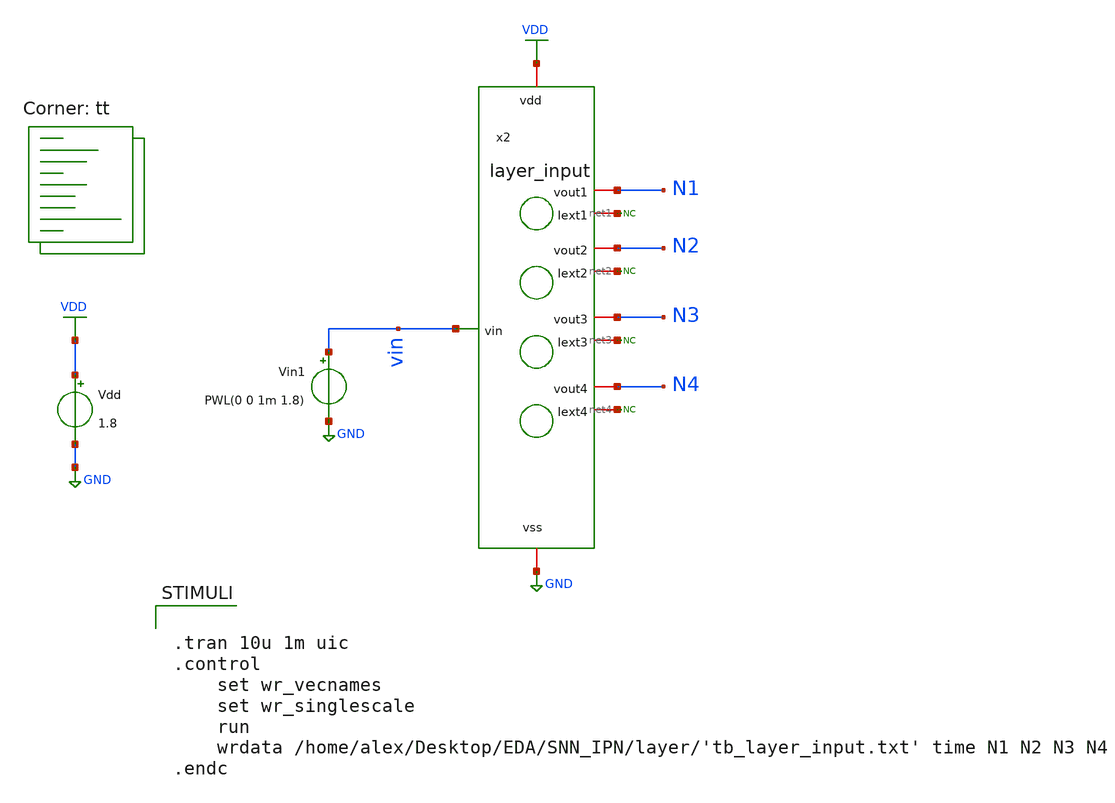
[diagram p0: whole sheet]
** sch_path: layer/tb_layer_input.sch
**.subckt tb_layer_input
x2 VDD GND vin N1 N2 N3 N4 net1 net2 net3 net4 layer_input
Vin1 vin GND PWL(0 0 1m 1.8)
* noconn #net1
* noconn #net2
* noconn #net3
* noconn #net4
Vdd VDD GND 1.8
**** begin user architecture code
.lib $::SKYWATER_MODELS/sky130.lib.spice tt
**** end user architecture code
**.ends

* expanding   symbol:  layer/layer_input.sym # of pins=11
** sym_path: layer/layer_input.sym
** sch_path: layer/layer_input.sch
.subckt layer_input vdd vss vin vout1 vout2 vout3 vout4 Iext1 Iext2 Iext3 Iext4
*.iopin vdd
*.iopin vss
*.ipin vin
*.iopin vout1
*.iopin vout2
*.iopin vout3
*.iopin vout4
*.ipin Iext1
*.ipin Iext2
*.ipin Iext3
*.ipin Iext4
x6 Iext1 vdd vg100n vout1 net1 vss ul_tun
x4 vdd vin Iext3 vss syn_pos
x8 vdd vin Iext1 vss syn_neg
I9 vg100n vss 100nA
XM4 vg100n vg100n vdd vdd sky130_fd_pr__pfet_01v8 L=0.15 W=2 nf=1 ad='int((nf+1)/2) * W/nf * 0.29' as='int((nf+2)/2) * W/nf * 0.29'
+ pd='2*int((nf+1)/2) * (W/nf + 0.29)' ps='2*int((nf+2)/2) * (W/nf + 0.29)' nrd='0.29 / W' nrs='0.29 / W'
+ sa=0 sb=0 sd=0 mult=1 m=1
XM1 net1 vileak vss vss sky130_fd_pr__nfet_01v8 L=0.15 W=1 nf=1 ad='int((nf+1)/2) * W/nf * 0.29' as='int((nf+2)/2) * W/nf * 0.29'
+ pd='2*int((nf+1)/2) * (W/nf + 0.29)' ps='2*int((nf+2)/2) * (W/nf + 0.29)' nrd='0.29 / W' nrs='0.29 / W'
+ sa=0 sb=0 sd=0 mult=1 m=1
XM2 vileak vileak vss vss sky130_fd_pr__nfet_01v8 L=0.15 W=10 nf=1 ad='int((nf+1)/2) * W/nf * 0.29' as='int((nf+2)/2) * W/nf * 0.29'
+ pd='2*int((nf+1)/2) * (W/nf + 0.29)' ps='2*int((nf+2)/2) * (W/nf + 0.29)' nrd='0.29 / W' nrs='0.29 / W'
+ sa=0 sb=0 sd=0 mult=1 m=1
I1 vdd vileak 100nA
x1 Iext2 vdd vg100n vout2 net2 vss ul_tun
x2 vdd vin Iext2 vss syn_neg
XM3 net2 vileak vss vss sky130_fd_pr__nfet_01v8 L=0.15 W=2 nf=1 ad='int((nf+1)/2) * W/nf * 0.29' as='int((nf+2)/2) * W/nf * 0.29'
+ pd='2*int((nf+1)/2) * (W/nf + 0.29)' ps='2*int((nf+2)/2) * (W/nf + 0.29)' nrd='0.29 / W' nrs='0.29 / W'
+ sa=0 sb=0 sd=0 mult=1 m=1
x3 Iext3 vdd vg100n vout3 net3 vss ul_tun
XM5 net3 vileak vss vss sky130_fd_pr__nfet_01v8 L=0.15 W=1 nf=1 ad='int((nf+1)/2) * W/nf * 0.29' as='int((nf+2)/2) * W/nf * 0.29'
+ pd='2*int((nf+1)/2) * (W/nf + 0.29)' ps='2*int((nf+2)/2) * (W/nf + 0.29)' nrd='0.29 / W' nrs='0.29 / W'
+ sa=0 sb=0 sd=0 mult=1 m=1
x7 vdd vin Iext4 vss syn_pos
x9 Iext4 vdd vg100n vout4 net4 vss ul_tun
XM6 net4 vileak vss vss sky130_fd_pr__nfet_01v8 L=0.15 W=2 nf=1 ad='int((nf+1)/2) * W/nf * 0.29' as='int((nf+2)/2) * W/nf * 0.29'
+ pd='2*int((nf+1)/2) * (W/nf + 0.29)' ps='2*int((nf+2)/2) * (W/nf + 0.29)' nrd='0.29 / W' nrs='0.29 / W'
+ sa=0 sb=0 sd=0 mult=1 m=1
.ends


* expanding   symbol:  Neuron/ultralif/ul_tun.sym # of pins=6
** sym_path: Neuron/ultralif/ul_tun.sym
** sch_path: Neuron/ultralif/ul_tun.sch
.subckt ul_tun Iext vdd g100n vout Ileak vss
*.iopin Iext
*.iopin vout
*.iopin vss
*.iopin Ileak
*.iopin vdd
*.iopin g100n
XM1 Ileak Ileak net1 vdd sky130_fd_pr__pfet_01v8 L=10 W=1 nf=1 ad='int((nf+1)/2) * W/nf * 0.29' as='int((nf+2)/2) * W/nf * 0.29'
+ pd='2*int((nf+1)/2) * (W/nf + 0.29)' ps='2*int((nf+2)/2) * (W/nf + 0.29)' nrd='0.29 / W' nrs='0.29 / W'
+ sa=0 sb=0 sd=0 mult=1 m=1
XM2 Ileak net2 net1 vdd sky130_fd_pr__pfet_01v8 L=0.15 W=1.5 nf=1 ad='int((nf+1)/2) * W/nf * 0.29' as='int((nf+2)/2) * W/nf * 0.29'
+ pd='2*int((nf+1)/2) * (W/nf + 0.29)' ps='2*int((nf+2)/2) * (W/nf + 0.29)' nrd='0.29 / W' nrs='0.29 / W'
+ sa=0 sb=0 sd=0 mult=1 m=1
XM3 net2 net2 net1 vdd sky130_fd_pr__pfet_01v8 L=0.15 W=15 nf=1 ad='int((nf+1)/2) * W/nf * 0.29' as='int((nf+2)/2) * W/nf * 0.29'
+ pd='2*int((nf+1)/2) * (W/nf + 0.29)' ps='2*int((nf+2)/2) * (W/nf + 0.29)' nrd='0.29 / W' nrs='0.29 / W'
+ sa=0 sb=0 sd=0 mult=1 m=1
XM4 net2 Ileak vss vss sky130_fd_pr__nfet_01v8 L=4 W=1 nf=1 ad='int((1 + 1)/2) * 1 / 1 * 0.29' as='int((1 + 2)/2) * 1 / 1 * 0.29'
+ pd='2*int((1 + 1)/2) * (1 / 1 + 0.29)' ps='2*int((1 + 2)/2) * (1 / 1 + 0.29)' nrd='0.29 / 1 ' nrs='0.29 / 1 '
+ sa=0 sb=0 sd=0 mult=1 m=1
C1 net1 vss 1p m=1
XM5 vout_n Ileak vss vss sky130_fd_pr__nfet_01v8 L=0.15 W=1 nf=1 ad='int((1 + 1)/2) * 1 / 1 * 0.29' as='int((1 + 2)/2) * 1 / 1 * 0.29'
+ pd='2*int((1 + 1)/2) * (1 / 1 + 0.29)' ps='2*int((1 + 2)/2) * (1 / 1 + 0.29)' nrd='0.29 / 1 ' nrs='0.29 / 1 '
+ sa=0 sb=0 sd=0 mult=1 m=1
XM6 vout_n g100n vdd vdd sky130_fd_pr__pfet_01v8 L=0.15 W=2 nf=1 ad='int((nf+1)/2) * W/nf * 0.29' as='int((nf+2)/2) * W/nf * 0.29'
+ pd='2*int((nf+1)/2) * (W/nf + 0.29)' ps='2*int((nf+2)/2) * (W/nf + 0.29)' nrd='0.29 / W' nrs='0.29 / W'
+ sa=0 sb=0 sd=0 mult=1 m=1
XM7 vout vout_n vss vss sky130_fd_pr__nfet_01v8 L=0.15 W=1 nf=1 ad='int((1 + 1)/2) * 1 / 1 * 0.29' as='int((1 + 2)/2) * 1 / 1 * 0.29'
+ pd='2*int((1 + 1)/2) * (1 / 1 + 0.29)' ps='2*int((1 + 2)/2) * (1 / 1 + 0.29)' nrd='0.29 / 1 ' nrs='0.29 / 1 '
+ sa=0 sb=0 sd=0 mult=1 m=1
XM8 vout vout_n vdd vdd sky130_fd_pr__pfet_01v8 L=0.15 W=2 nf=1 ad='int((nf+1)/2) * W/nf * 0.29' as='int((nf+2)/2) * W/nf * 0.29'
+ pd='2*int((nf+1)/2) * (W/nf + 0.29)' ps='2*int((nf+2)/2) * (W/nf + 0.29)' nrd='0.29 / W' nrs='0.29 / W'
+ sa=0 sb=0 sd=0 mult=1 m=1
vext Iext net1 0
**** begin user architecture code


.save i(vext)


**** end user architecture code
.ends


* expanding   symbol:  Neuron/ultralif/syn_pos.sym # of pins=4
** sym_path: Neuron/ultralif/syn_pos.sym
** sch_path: Neuron/ultralif/syn_pos.sch
.subckt syn_pos vdd Vin Isyn vss
*.iopin Vin
*.iopin vdd
*.iopin vss
*.iopin Isyn
XM9 Isyn vx vdd vdd sky130_fd_pr__pfet_01v8 L=1 W=0.5 nf=1 ad='int((nf+1)/2) * W/nf * 0.29' as='int((nf+2)/2) * W/nf * 0.29'
+ pd='2*int((nf+1)/2) * (W/nf + 0.29)' ps='2*int((nf+2)/2) * (W/nf + 0.29)' nrd='0.29 / W' nrs='0.29 / W'
+ sa=0 sb=0 sd=0 mult=1 m=1
XM10 vx vx vdd vdd sky130_fd_pr__pfet_01v8 L=0.15 W=0.5 nf=1 ad='int((nf+1)/2) * W/nf * 0.29' as='int((nf+2)/2) * W/nf * 0.29'
+ pd='2*int((nf+1)/2) * (W/nf + 0.29)' ps='2*int((nf+2)/2) * (W/nf + 0.29)' nrd='0.29 / W' nrs='0.29 / W'
+ sa=0 sb=0 sd=0 mult=5 m=5
XM12 vx Vin vss vss sky130_fd_pr__nfet_01v8 L=1 W=0.4 nf=1 ad='int((1 + 1)/2) * 0.4 / 1 * 0.29' as='int((1 + 2)/2) * 0.4 / 1 * 0.29'
+ pd='2*int((1 + 1)/2) * (0.4 / 1 + 0.29)' ps='2*int((1 + 2)/2) * (0.4 / 1 + 0.29)' nrd='0.29 / 0.4 ' nrs='0.29 / 0.4 '
+ sa=0 sb=0 sd=0 mult=1 m=1
.ends


* expanding   symbol:  Neuron/ultralif/syn_neg.sym # of pins=4
** sym_path: Neuron/ultralif/syn_neg.sym
** sch_path: Neuron/ultralif/syn_neg.sch
.subckt syn_neg vdd Vin Isyn vss
*.iopin Vin
*.iopin Isyn
*.iopin vdd
*.iopin vss
XM10 Isyn Vin vx vdd sky130_fd_pr__pfet_01v8 L=35 W=0.5 nf=1 ad='int((nf+1)/2) * W/nf * 0.29' as='int((nf+2)/2) * W/nf * 0.29'
+ pd='2*int((nf+1)/2) * (W/nf + 0.29)' ps='2*int((nf+2)/2) * (W/nf + 0.29)' nrd='0.29 / W' nrs='0.29 / W'
+ sa=0 sb=0 sd=0 mult=1 m=1
XM1 vx Vin vdd vdd sky130_fd_pr__pfet_01v8 L=35 W=0.5 nf=1 ad='int((nf+1)/2) * W/nf * 0.29' as='int((nf+2)/2) * W/nf * 0.29'
+ pd='2*int((nf+1)/2) * (W/nf + 0.29)' ps='2*int((nf+2)/2) * (W/nf + 0.29)' nrd='0.29 / W' nrs='0.29 / W'
+ sa=0 sb=0 sd=0 mult=1 m=1
XM2 Isyn net1 vdd vdd sky130_fd_pr__pfet_01v8 L=1 W=0.5 nf=1 ad='int((nf+1)/2) * W/nf * 0.29' as='int((nf+2)/2) * W/nf * 0.29'
+ pd='2*int((nf+1)/2) * (W/nf + 0.29)' ps='2*int((nf+2)/2) * (W/nf + 0.29)' nrd='0.29 / W' nrs='0.29 / W'
+ sa=0 sb=0 sd=0 mult=1 m=1
XR1 net1 vdd sky130_fd_pr__res_generic_po W=1.15 L=1 m=1
XR2 vss net1 sky130_fd_pr__res_generic_po W=1 L=1 m=1
.ends

.GLOBAL GND
.GLOBAL VDD
**** begin user architecture code


.tran 10u 1m uic
.control
	set wr_vecnames
	set wr_singlescale
	run
	wrdata /home/alex/Desktop/EDA/SNN_IPN/layer/'tb_layer_input.txt' time N1 N2 N3 N4
.endc


**** end user architecture code
.end
